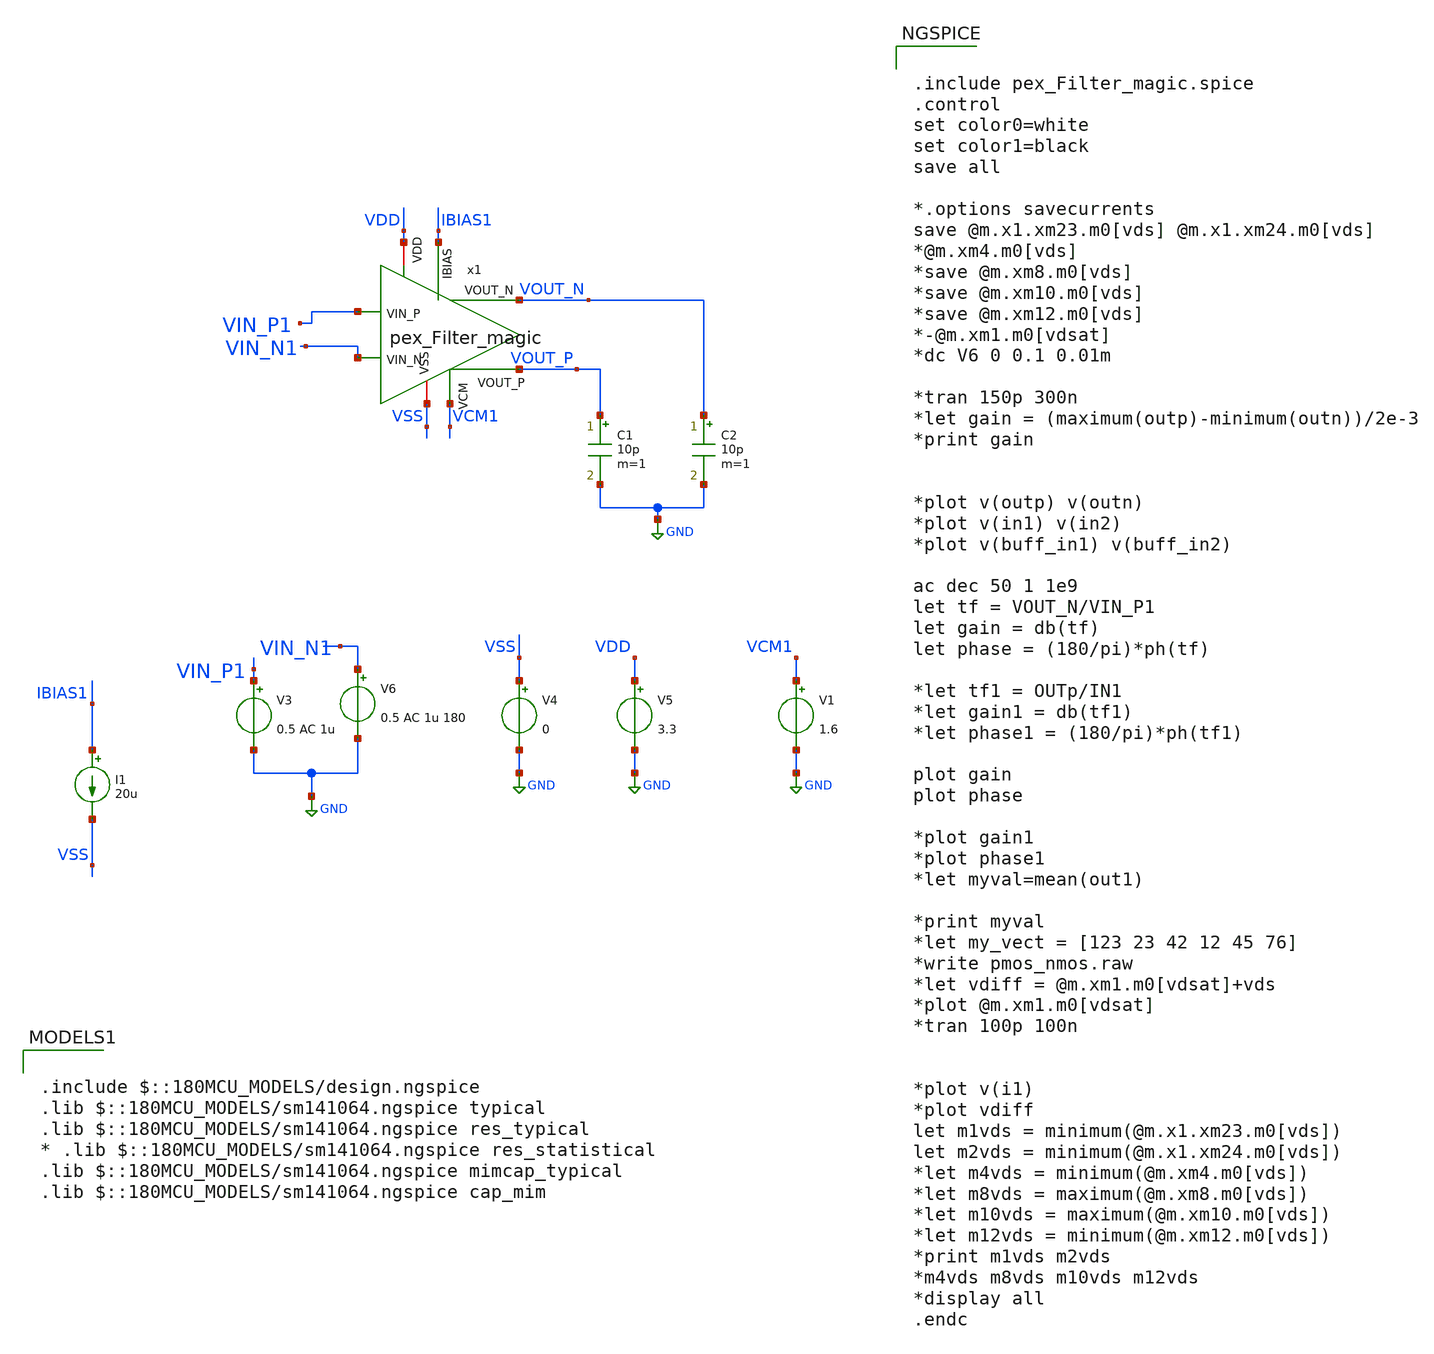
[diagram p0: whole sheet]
** sch_path: AWG_OUTPUT_AND_MUX_PAKISTAN_05/xschem/PEX_FILTER_TB.sch
**.subckt PEX_FILTER_TB
V3 VIN_P1 GND 0.5 AC 1u
V4 VSS GND 0
V5 VDD GND 3.3
V6 VIN_N1 GND 0.5 AC 1u 180
I1 IBIAS1 VSS 20u
C1 VOUT_P GND 10p m=1
C2 VOUT_N GND 10p m=1
V1 VCM1 GND 1.6
x1 VIN_N1 VIN_P1 VOUT_P VOUT_N VDD IBIAS1 VCM1 VSS pex_Filter_magic
**** begin user architecture code


.include pex_Filter_magic.spice
.control
set color0=white
set color1=black
save all

*.options savecurrents
save @m.x1.xm23.m0[vds] @m.x1.xm24.m0[vds]
*@m.xm4.m0[vds]
*save @m.xm8.m0[vds]
*save @m.xm10.m0[vds]
*save @m.xm12.m0[vds]
*-@m.xm1.m0[vdsat]
*dc V6 0 0.1 0.01m

*tran 150p 300n
*let gain = (maximum(outp)-minimum(outn))/2e-3
*print gain


*plot v(outp) v(outn)
*plot v(in1) v(in2)
*plot v(buff_in1) v(buff_in2)

ac dec 50 1 1e9
let tf = VOUT_N/VIN_P1
let gain = db(tf)
let phase = (180/pi)*ph(tf)

*let tf1 = OUTp/IN1
*let gain1 = db(tf1)
*let phase1 = (180/pi)*ph(tf1)

plot gain
plot phase

*plot gain1
*plot phase1
*let myval=mean(out1)

*print myval
*let my_vect = [123 23 42 12 45 76]
*write pmos_nmos.raw
*let vdiff = @m.xm1.m0[vdsat]+vds
*plot @m.xm1.m0[vdsat]
*tran 100p 100n


*plot v(i1)
*plot vdiff
let m1vds = minimum(@m.x1.xm23.m0[vds])
let m2vds = minimum(@m.x1.xm24.m0[vds])
*let m4vds = minimum(@m.xm4.m0[vds])
*let m8vds = maximum(@m.xm8.m0[vds])
*let m10vds = maximum(@m.xm10.m0[vds])
*let m12vds = minimum(@m.xm12.m0[vds])
*print m1vds m2vds
*m4vds m8vds m10vds m12vds
*display all
.endc



.include $::180MCU_MODELS/design.ngspice
.lib $::180MCU_MODELS/sm141064.ngspice typical
.lib $::180MCU_MODELS/sm141064.ngspice res_typical
* .lib $::180MCU_MODELS/sm141064.ngspice res_statistical
.lib $::180MCU_MODELS/sm141064.ngspice mimcap_typical
.lib $::180MCU_MODELS/sm141064.ngspice cap_mim

**** end user architecture code
**.ends
.GLOBAL GND
.end
